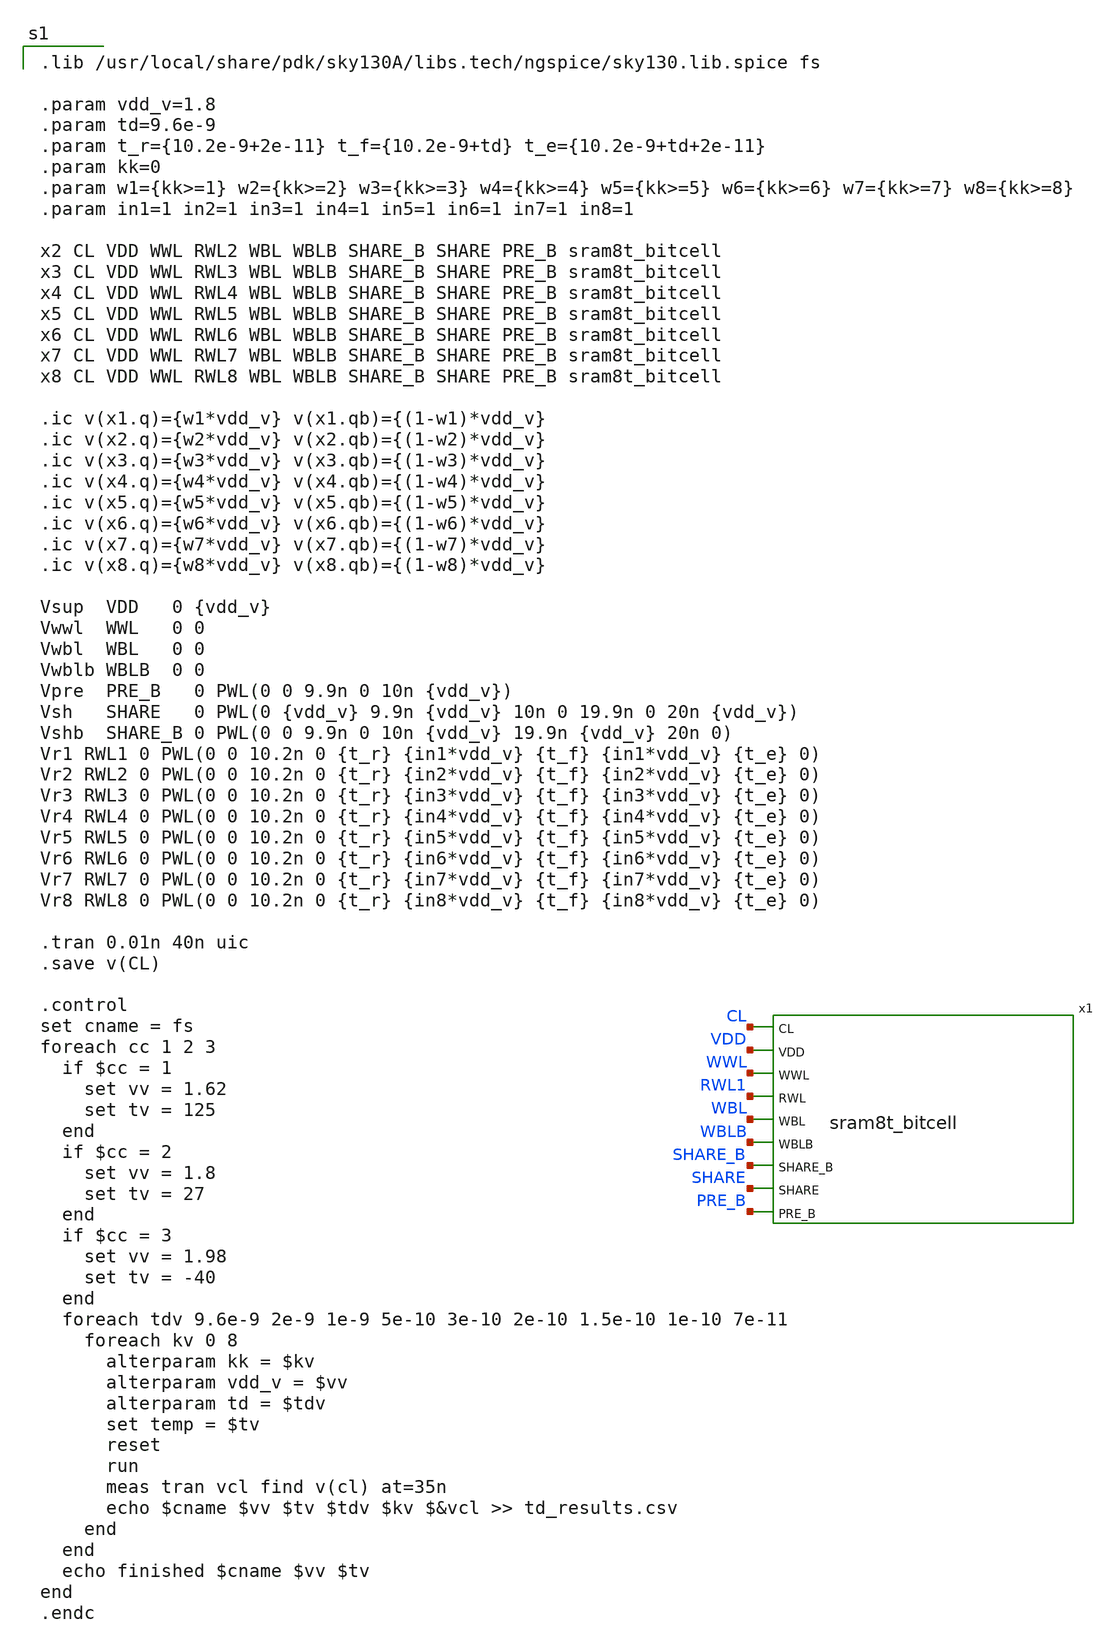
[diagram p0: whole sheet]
** sch_path: schematics/untitled.sch
**.subckt untitled
x1 CL VDD WWL RWL1 WBL WBLB SHARE_B SHARE PRE_B sram8t_bitcell
**** begin user architecture code

.lib /usr/local/share/pdk/sky130A/libs.tech/ngspice/sky130.lib.spice fs

.param vdd_v=1.8
.param td=9.6e-9
.param t_r={10.2e-9+2e-11} t_f={10.2e-9+td} t_e={10.2e-9+td+2e-11}
.param kk=0
.param w1={kk>=1} w2={kk>=2} w3={kk>=3} w4={kk>=4} w5={kk>=5} w6={kk>=6} w7={kk>=7} w8={kk>=8}
.param in1=1 in2=1 in3=1 in4=1 in5=1 in6=1 in7=1 in8=1

x2 CL VDD WWL RWL2 WBL WBLB SHARE_B SHARE PRE_B sram8t_bitcell
x3 CL VDD WWL RWL3 WBL WBLB SHARE_B SHARE PRE_B sram8t_bitcell
x4 CL VDD WWL RWL4 WBL WBLB SHARE_B SHARE PRE_B sram8t_bitcell
x5 CL VDD WWL RWL5 WBL WBLB SHARE_B SHARE PRE_B sram8t_bitcell
x6 CL VDD WWL RWL6 WBL WBLB SHARE_B SHARE PRE_B sram8t_bitcell
x7 CL VDD WWL RWL7 WBL WBLB SHARE_B SHARE PRE_B sram8t_bitcell
x8 CL VDD WWL RWL8 WBL WBLB SHARE_B SHARE PRE_B sram8t_bitcell

.ic v(x1.q)={w1*vdd_v} v(x1.qb)={(1-w1)*vdd_v}
.ic v(x2.q)={w2*vdd_v} v(x2.qb)={(1-w2)*vdd_v}
.ic v(x3.q)={w3*vdd_v} v(x3.qb)={(1-w3)*vdd_v}
.ic v(x4.q)={w4*vdd_v} v(x4.qb)={(1-w4)*vdd_v}
.ic v(x5.q)={w5*vdd_v} v(x5.qb)={(1-w5)*vdd_v}
.ic v(x6.q)={w6*vdd_v} v(x6.qb)={(1-w6)*vdd_v}
.ic v(x7.q)={w7*vdd_v} v(x7.qb)={(1-w7)*vdd_v}
.ic v(x8.q)={w8*vdd_v} v(x8.qb)={(1-w8)*vdd_v}

Vsup  VDD   0 {vdd_v}
Vwwl  WWL   0 0
Vwbl  WBL   0 0
Vwblb WBLB  0 0
Vpre  PRE_B   0 PWL(0 0 9.9n 0 10n {vdd_v})
Vsh   SHARE   0 PWL(0 {vdd_v} 9.9n {vdd_v} 10n 0 19.9n 0 20n {vdd_v})
Vshb  SHARE_B 0 PWL(0 0 9.9n 0 10n {vdd_v} 19.9n {vdd_v} 20n 0)
Vr1 RWL1 0 PWL(0 0 10.2n 0 {t_r} {in1*vdd_v} {t_f} {in1*vdd_v} {t_e} 0)
Vr2 RWL2 0 PWL(0 0 10.2n 0 {t_r} {in2*vdd_v} {t_f} {in2*vdd_v} {t_e} 0)
Vr3 RWL3 0 PWL(0 0 10.2n 0 {t_r} {in3*vdd_v} {t_f} {in3*vdd_v} {t_e} 0)
Vr4 RWL4 0 PWL(0 0 10.2n 0 {t_r} {in4*vdd_v} {t_f} {in4*vdd_v} {t_e} 0)
Vr5 RWL5 0 PWL(0 0 10.2n 0 {t_r} {in5*vdd_v} {t_f} {in5*vdd_v} {t_e} 0)
Vr6 RWL6 0 PWL(0 0 10.2n 0 {t_r} {in6*vdd_v} {t_f} {in6*vdd_v} {t_e} 0)
Vr7 RWL7 0 PWL(0 0 10.2n 0 {t_r} {in7*vdd_v} {t_f} {in7*vdd_v} {t_e} 0)
Vr8 RWL8 0 PWL(0 0 10.2n 0 {t_r} {in8*vdd_v} {t_f} {in8*vdd_v} {t_e} 0)

.tran 0.01n 40n uic
.save v(CL)

.control
set cname = fs
foreach cc 1 2 3
  if $cc = 1
    set vv = 1.62
    set tv = 125
  end
  if $cc = 2
    set vv = 1.8
    set tv = 27
  end
  if $cc = 3
    set vv = 1.98
    set tv = -40
  end
  foreach tdv 9.6e-9 2e-9 1e-9 5e-10 3e-10 2e-10 1.5e-10 1e-10 7e-11
    foreach kv 0 8
      alterparam kk = $kv
      alterparam vdd_v = $vv
      alterparam td = $tdv
      set temp = $tv
      reset
      run
      meas tran vcl find v(cl) at=35n
      echo $cname $vv $tv $tdv $kv $&vcl >> td_results.csv
    end
  end
  echo finished $cname $vv $tv
end
.endc

**** end user architecture code
**.ends
.end
